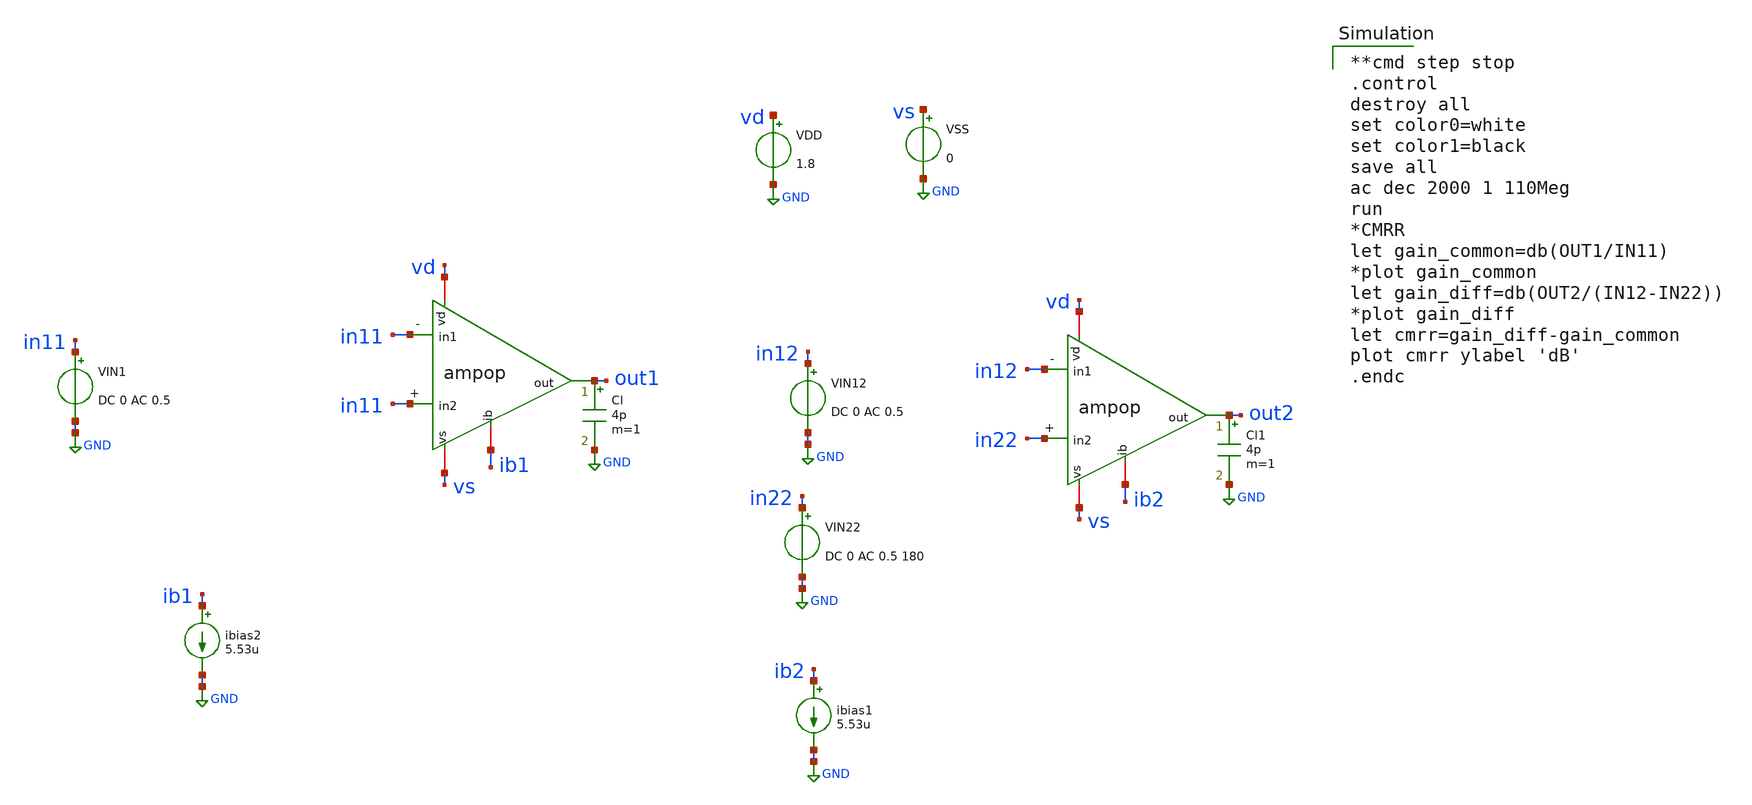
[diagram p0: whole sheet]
** sch_path: amp-op/xschem/ampop_tb-CMRR.sch
* Copyright 2020 Stefan Frederik Schippers
* Licensed under the Apache License, Version 2.0 (the "License");
* you may not use this file except in compliance with the License.
* You may obtain a copy of the License at
* https://www.apache.org/licenses/LICENSE-2.0
* Unless required by applicable law or agreed to in writing, software
* distributed under the License is distributed on an "AS IS" BASIS,
* WITHOUT WARRANTIES OR CONDITIONS OF ANY KIND, either express or implied.
* See the License for the specific language governing permissions and
* limitations under the License.
**.subckt ampop_tb-CMRR
ibias2 ib1 GND 5.53u
VDD vd GND 1.8
VSS vs GND 0
VIN12 in12 GND DC 0 AC 0.5
ibias1 ib2 GND 5.53u
VIN22 in22 GND DC 0 AC 0.5 180
Cl out1 GND 4p m=1
x1 vd in11 in11 out1 ib1 vs ampop
Cl1 out2 GND 4p m=1
x2 vd in12 in22 out2 ib2 vs ampop
VIN1 in11 GND DC 0 AC 0.5
**** begin user architecture code

**cmd step stop
.control
destroy all
set color0=white
set color1=black
save all
ac dec 2000 1 110Meg
run
*CMRR
let gain_common=db(OUT1/IN11)
*plot gain_common
let gain_diff=db(OUT2/(IN12-IN22))
*plot gain_diff
let cmrr=gain_diff-gain_common
plot cmrr ylabel 'dB'
.endc

 .lib $::SKYWATER_MODELS/sky130.lib.spice tt
.include $::SKYWATER_STDCELLS/sky130_fd_sc_hd.spice

**** end user architecture code
**.ends

* expanding   symbol:  /home/hugodg/projects-sky130/temp-sensor/amp-op/xschem/ampop.sym # of pins=6
** sym_path: amp-op/xschem/ampop.sym
** sch_path: amp-op/xschem/ampop.sch
.subckt ampop vd in1 in2 out ib vs
*.iopin vd
*.opin out
*.ipin in1
*.ipin in2
*.iopin vs
*.iopin ib
X1 vd net1 out ib vs buffer
X2 vd ib net1 in2 in1 vs ota
**** begin user architecture code


R0 in1 in1.t0 88.243
R1 in2 in2.t0 88.786
R2 vs.n0 vs.n4 362.164
R3 vs.n0 vs.n2 362.164
R4 vs.n30 vs.n25 181.834
R5 vs.n14 vs.n9 181.834
R6 vs.n18 vs.n17 108.422
R7 vs.n31 vs.n30 108.422
R8 vs.n0 vs.n6 108.422
R9 vs.n15 vs.n14 108.422
R10 vs.n34 vs.n5 5.045
R11 vs.n5 vs 0.812
R12 vs vs 0.431
R13 vs.n34 vs.n33 0.202
R14 vs vs.n34 0.182
R15 vs.n19 vs.n16 0.15
R16 vs.n32 vs.n23 0.062
R17 vs.n20 vs.n19 0.057
R18 vs.n16 vs.n7 0.055
R19 vs.n25 vs.n24 0.046
R20 vs.n9 vs.n8 0.046
R21 vs.n30 vs.n29 0.042
R22 vs.n14 vs.n13 0.042
R23 vs.n28 vs.n27 0.035
R24 vs.n12 vs.n11 0.035
R25 vs.n27 vs.n26 0.025
R26 vs.n11 vs.n10 0.025
R27 vs.n29 vs.n28 0.025
R28 vs.n13 vs.n12 0.025
R29 vs.n16 vs.n15 0.017
R30 vs.n19 vs.n18 0.017
R31 vs.n32 vs.n31 0.017
R32 vs.n4 vs.n3 0.013
R33 vs.n2 vs.n1 0.013
R34 vs.n7 vs.n0 0.007
R35 vs vs 0.005
R36 vs.n23 vs.n20 0.004
R37 vs.n33 vs.n32 0.003
R38 vs.n5 vs 0.002
R39 vs.n22 vs.n21 0.001
R40 vs.n23 vs.n22 0.001
R41 ib.n5 ib.t6 196.205
R42 ib.n6 ib.t5 196.185
R43 ib.n7 ib.t8 196.183
R44 ib.n8 ib.t7 196.181
R45 ib.n4 ib.t2 160.591
R46 ib.t2 ib.n3 160.08
R47 ib.n4 ib.t4 160.055
R48 ib.n0 ib.t9 24.837
R49 ib.n0 ib.t0 24.107
R50 ib.n1 ib.t1 17.747
R51 ib.n3 ib.t3 5.789
R52 ib.n2 ib.n1 4.041
R53 ib ib.n8 3.3
R54 ib.n5 ib.n4 1.125
R55 ib.n3 ib 0.407
R56 ib.n1 ib.n0 0.387
R57 ib.n6 ib.n5 0.175
R58 ib.n8 ib.n7 0.168
R59 ib.n7 ib.n6 0.162
R60 ib.n2 ib 0.113
R61 ib ib.n2 0.078
R62 vd.n74 vd.n73 5396.47
R63 vd.n63 vd.n62 3501.18
R64 vd.n84 vd.n83 3501.18
R65 vd.n62 vd.n59 909.81
R66 vd.n83 vd.n80 909.81
R67 vd.n65 vd.n64 722.167
R68 vd.n86 vd.n85 722.167
R69 vd.n71 vd.n70 575.623
R70 vd.n75 vd.n70 575.623
R71 vd.n74 vd.n69 569.784
R72 vd.n72 vd.n71 515.374
R73 vd.n53 vd.n52 379.482
R74 vd.n40 vd.n34 379.482
R75 vd.n61 vd.n60 373.458
R76 vd.n65 vd.n60 373.458
R77 vd.n82 vd.n81 373.458
R78 vd.n86 vd.n81 373.458
R79 vd.n69 vd.n68 326.776
R80 vd.n54 vd.n53 297.411
R81 vd.n41 vd.n40 297.411
R82 vd.n59 vd.n58 270.305
R83 vd.n80 vd.n79 270.305
R84 vd.n76 vd.n75 251.205
R85 vd.n71 vd.n68 248.846
R86 vd.n19 vd.n16 131.387
R87 vd.n4 vd.n1 131.387
R88 vd.n24 vd.n21 131.011
R89 vd.n9 vd.n6 131.011
R90 vd.n66 vd.n65 105.107
R91 vd.n87 vd.n86 105.107
R92 vd.n61 vd.n58 103.152
R93 vd.n82 vd.n79 103.152
R94 vd.n29 vd.n24 54.211
R95 vd.n14 vd.n9 54.211
R96 vd.n29 vd.n19 53.835
R97 vd.n14 vd.n4 53.835
R98 vd.n57 vd.n14 8.271
R99 vd.n57 vd.n29 7.938
R100 vd.n57 vd.n56 4.028
R101 vd.n91 vd.n90 1.897
R102 vd.n77 vd.n76 1.606
R103 vd.n67 vd.n66 1.199
R104 vd.n88 vd.n87 1.199
R105 vd.n91 vd.n57 1.058
R106 vd vd.n89 1.008
R107 vd.n78 vd.n77 0.975
R108 vd vd.n88 0.594
R109 vd.n77 vd.n68 0.389
R110 vd.n67 vd.n58 0.389
R111 vd.n88 vd.n79 0.334
R112 vd.n55 vd.n45 0.296
R113 vd.n89 vd.n78 0.273
R114 vd.n42 vd.n32 0.228
R115 vd.n56 vd.n55 0.18
R116 vd.n89 vd 0.173
R117 vd.n56 vd.n42 0.167
R118 vd.n19 vd.n18 0.161
R119 vd.n24 vd.n23 0.161
R120 vd.n4 vd.n3 0.161
R121 vd.n9 vd.n8 0.161
R122 vd.n23 vd.n22 0.139
R123 vd.n8 vd.n7 0.139
R124 vd.n18 vd.n17 0.139
R125 vd.n3 vd.n2 0.139
R126 vd.n90 vd 0.071
R127 vd.n78 vd.n67 0.054
R128 vd vd.n91 0.044
R129 vd.n90 vd 0.034
R130 vd.n42 vd.n41 0.017
R131 vd.n55 vd.n54 0.017
R132 vd.n62 vd.n61 0.015
R133 vd.n83 vd.n82 0.015
R134 vd.n16 vd.n15 0.015
R135 vd.n21 vd.n20 0.015
R136 vd.n1 vd.n0 0.015
R137 vd.n6 vd.n5 0.015
R138 vd.n52 vd.n51 0.013
R139 vd.n34 vd.n33 0.013
R140 vd.n26 vd.n25 0.013
R141 vd.n27 vd.n26 0.013
R142 vd.n11 vd.n10 0.013
R143 vd.n12 vd.n11 0.013
R144 vd.n75 vd.n74 0.004
R145 vd.n73 vd.n72 0.003
R146 vd.n63 vd.n60 0.003
R147 vd.n84 vd.n81 0.003
R148 vd.n53 vd.n50 0.003
R149 vd.n47 vd.n46 0.003
R150 vd.n36 vd.n35 0.003
R151 vd.n40 vd.n39 0.003
R152 vd.n64 vd.n63 0.003
R153 vd.n85 vd.n84 0.003
R154 vd.n50 vd.n49 0.003
R155 vd.n37 vd.n36 0.003
R156 vd.n48 vd.n47 0.003
R157 vd.n39 vd.n38 0.003
R158 vd.n73 vd.n70 0.003
R159 vd.n49 vd.n48 0.002
R160 vd.n38 vd.n37 0.002
R161 vd.n29 vd.n28 0.002
R162 vd.n28 vd.n27 0.002
R163 vd.n14 vd.n13 0.002
R164 vd.n13 vd.n12 0.002
R165 vd.n72 vd.n69 0.001
R166 vd.n64 vd.n59 0.001
R167 vd.n85 vd.n80 0.001
R168 vd.n32 vd.n31 0.001
R169 vd.n45 vd.n44 0.001
R170 vd.n44 vd.n43 0.001
R171 vd.n31 vd.n30 0.001
R172 vd.n76 vd.n69 0.001
R173 vd.n66 vd.n59 0.001
R174 vd.n87 vd.n80 0.001
R175 out.t0 out.n7 175.091
R176 out.n0 out.t2 175.044
R177 out.n2 out.n1 150.491
R178 out.n4 out.n3 150.491
R179 out.n6 out.n5 141.106
R180 out out.t0 28.743
R181 out.n5 out.t1 24.103
R182 out.n6 out.t7 24.103
R183 out.n4 out.t5 24.103
R184 out.n2 out.t3 24.102
R185 out.n0 out.t6 24.102
R186 out.n1 out.t9 24.102
R187 out.n3 out.t4 24.102
R188 out.n7 out.t8 24.102
R189 out.n7 out.n6 1.085
R190 out.n3 out.n2 0.988
R191 out.n5 out.n4 0.913
R192 out.n1 out.n0 0.863
R193 out out 0.023
R194 buffer_0/net1.n4 buffer_0/net1.t29 172.218
R195 buffer_0/net1.n5 buffer_0/net1.n4 149.523
R196 buffer_0/net1.n6 buffer_0/net1.n5 149.523
R197 buffer_0/net1.n7 buffer_0/net1.n6 149.523
R198 buffer_0/net1.n8 buffer_0/net1.n7 149.523
R199 buffer_0/net1.n9 buffer_0/net1.n8 149.523
R200 buffer_0/net1.n10 buffer_0/net1.n9 149.523
R201 buffer_0/net1.n11 buffer_0/net1.n10 149.523
R202 buffer_0/net1.n12 buffer_0/net1.n11 149.523
R203 buffer_0/net1.n13 buffer_0/net1.n12 149.523
R204 buffer_0/net1.n14 buffer_0/net1.n13 149.523
R205 buffer_0/net1.n15 buffer_0/net1.n14 149.523
R206 buffer_0/net1.n16 buffer_0/net1.n15 149.523
R207 buffer_0/net1.n17 buffer_0/net1.n16 149.523
R208 buffer_0/net1.n18 buffer_0/net1.n17 149.523
R209 buffer_0/net1.n19 buffer_0/net1.n18 149.523
R210 buffer_0/net1.n20 buffer_0/net1.n19 149.523
R211 buffer_0/net1.n21 buffer_0/net1.n20 149.523
R212 buffer_0/net1.n22 buffer_0/net1.n21 148.639
R213 buffer_0/net1.n22 buffer_0/net1.t16 24.284
R214 buffer_0/net1.n21 buffer_0/net1.t10 24.101
R215 buffer_0/net1.n20 buffer_0/net1.t27 24.101
R216 buffer_0/net1.n19 buffer_0/net1.t21 24.101
R217 buffer_0/net1.n18 buffer_0/net1.t4 24.101
R218 buffer_0/net1.n17 buffer_0/net1.t0 24.101
R219 buffer_0/net1.n16 buffer_0/net1.t22 24.101
R220 buffer_0/net1.n15 buffer_0/net1.t26 24.101
R221 buffer_0/net1.n14 buffer_0/net1.t18 24.101
R222 buffer_0/net1.n13 buffer_0/net1.t6 24.101
R223 buffer_0/net1.n12 buffer_0/net1.t23 24.101
R224 buffer_0/net1.n11 buffer_0/net1.t25 24.101
R225 buffer_0/net1.n10 buffer_0/net1.t8 24.101
R226 buffer_0/net1.n9 buffer_0/net1.t12 24.101
R227 buffer_0/net1.n8 buffer_0/net1.t28 24.101
R228 buffer_0/net1.n7 buffer_0/net1.t24 24.101
R229 buffer_0/net1.n6 buffer_0/net1.t14 24.101
R230 buffer_0/net1.n5 buffer_0/net1.t2 24.101
R231 buffer_0/net1.n4 buffer_0/net1.t20 24.101
R232 buffer_0/net1.n3 buffer_0/net1.t11 17.4
R233 buffer_0/net1.n3 buffer_0/net1.t17 17.4
R234 buffer_0/net1.n0 buffer_0/net1.t3 17.4
R235 buffer_0/net1.n0 buffer_0/net1.t15 17.4
R236 buffer_0/net1.n1 buffer_0/net1.t13 17.4
R237 buffer_0/net1.n1 buffer_0/net1.t9 17.4
R238 buffer_0/net1.n2 buffer_0/net1.t1 17.4
R239 buffer_0/net1.n2 buffer_0/net1.t5 17.4
R240 buffer_0/net1.n25 buffer_0/net1.t7 17.4
R241 buffer_0/net1.n25 buffer_0/net1.t19 17.4
R242 buffer_0/net1.n24 buffer_0/net1.n23 3.481
R243 buffer_0/net1 buffer_0/net1.n0 3.306
R244 buffer_0/net1.n27 buffer_0/net1.n26 3.218
R245 buffer_0/net1.n26 buffer_0/net1.n24 3.218
R246 buffer_0/net1.n23 buffer_0/net1.n22 1.24
R247 buffer_0/net1.n27 buffer_0/net1.n1 0.931
R248 buffer_0/net1.n24 buffer_0/net1.n2 0.931
R249 buffer_0/net1.n26 buffer_0/net1.n25 0.931
R250 buffer_0/net1 buffer_0/net1.n27 0.843
R251 buffer_0/net1.n23 buffer_0/net1.n3 0.389
C0 ota_0/m1_1300_5200# ota_0/out -0.03fF
C1 buffer_0/net2 vd 0.01fF
C2 ota_0/out vd 0.05fF
C3 buffer_0/net1.t3 vs 0.02fF
C4 buffer_0/net1.t15 vs 0.02fF
C5 buffer_0/net1.n0 vs 0.31fF $ **FLOATING
C6 buffer_0/net1.t13 vs 0.02fF
C7 buffer_0/net1.t9 vs 0.02fF
C8 buffer_0/net1.n1 vs 0.19fF $ **FLOATING
C9 buffer_0/net1.t1 vs 0.02fF
C10 buffer_0/net1.t5 vs 0.02fF
C11 buffer_0/net1.n2 vs 0.19fF $ **FLOATING
C12 buffer_0/net1.t11 vs 0.02fF
C13 buffer_0/net1.t17 vs 0.02fF
C14 buffer_0/net1.n3 vs 0.15fF $ **FLOATING
C15 buffer_0/net1.t10 vs 0.47fF
C16 buffer_0/net1.t27 vs 0.47fF
C17 buffer_0/net1.t21 vs 0.47fF
C18 buffer_0/net1.t4 vs 0.47fF
C19 buffer_0/net1.t0 vs 0.47fF
C20 buffer_0/net1.t22 vs 0.47fF
C21 buffer_0/net1.t26 vs 0.47fF
C22 buffer_0/net1.t18 vs 0.47fF
C23 buffer_0/net1.t6 vs 0.47fF
C24 buffer_0/net1.t23 vs 0.47fF
C25 buffer_0/net1.t25 vs 0.47fF
C26 buffer_0/net1.t8 vs 0.47fF
C27 buffer_0/net1.t12 vs 0.47fF
C28 buffer_0/net1.t28 vs 0.47fF
C29 buffer_0/net1.t24 vs 0.47fF
C30 buffer_0/net1.t14 vs 0.47fF
C31 buffer_0/net1.t2 vs 0.47fF
C32 buffer_0/net1.t20 vs 0.47fF
C33 buffer_0/net1.t29 vs 0.75fF
C34 buffer_0/net1.n4 vs 0.39fF $ **FLOATING
C35 buffer_0/net1.n5 vs 0.34fF $ **FLOATING
C36 buffer_0/net1.n6 vs 0.34fF $ **FLOATING
C37 buffer_0/net1.n7 vs 0.34fF $ **FLOATING
C38 buffer_0/net1.n8 vs 0.34fF $ **FLOATING
C39 buffer_0/net1.n9 vs 0.34fF $ **FLOATING
C40 buffer_0/net1.n10 vs 0.34fF $ **FLOATING
C41 buffer_0/net1.n11 vs 0.34fF $ **FLOATING
C42 buffer_0/net1.n12 vs 0.34fF $ **FLOATING
C43 buffer_0/net1.n13 vs 0.34fF $ **FLOATING
C44 buffer_0/net1.n14 vs 0.34fF $ **FLOATING
C45 buffer_0/net1.n15 vs 0.34fF $ **FLOATING
C46 buffer_0/net1.n16 vs 0.34fF $ **FLOATING
C47 buffer_0/net1.n17 vs 0.34fF $ **FLOATING
C48 buffer_0/net1.n18 vs 0.34fF $ **FLOATING
C49 buffer_0/net1.n19 vs 0.34fF $ **FLOATING
C50 buffer_0/net1.n20 vs 0.34fF $ **FLOATING
C51 buffer_0/net1.n21 vs 0.34fF $ **FLOATING
C52 buffer_0/net1.t16 vs 0.47fF
C53 buffer_0/net1.n22 vs 0.21fF $ **FLOATING
C54 buffer_0/net1.n23 vs 1.22fF $ **FLOATING
C55 buffer_0/net1.n24 vs 4.35fF $ **FLOATING
C56 buffer_0/net1.t7 vs 0.02fF
C57 buffer_0/net1.t19 vs 0.02fF
C58 buffer_0/net1.n25 vs 0.19fF $ **FLOATING
C59 buffer_0/net1.n26 vs 0.36fF $ **FLOATING
C60 buffer_0/net1.n27 vs 0.25fF $ **FLOATING
C61 out.t8 vs 0.59fF
C62 out.t1 vs 0.59fF
C63 out.t4 vs 0.59fF
C64 out.t9 vs 0.59fF
C65 out.t2 vs 0.94fF
C66 out.t6 vs 0.59fF
C67 out.n0 vs 2.69fF $ **FLOATING
C68 out.n1 vs 2.83fF $ **FLOATING
C69 out.t3 vs 0.59fF
C70 out.n2 vs 0.86fF $ **FLOATING
C71 out.n3 vs 0.86fF $ **FLOATING
C72 out.t5 vs 0.59fF
C73 out.n4 vs 0.91fF $ **FLOATING
C74 out.n5 vs 0.92fF $ **FLOATING
C75 out.t7 vs 0.59fF
C76 out.n6 vs 0.84fF $ **FLOATING
C77 out.n7 vs 0.91fF $ **FLOATING
C78 out.t0 vs 0.89fF
C79 vd.n0 vs 0.34fF $ **FLOATING
C80 vd.n1 vs 0.06fF $ **FLOATING
C81 vd.n2 vs 0.33fF $ **FLOATING
C82 vd.n3 vs 0.04fF $ **FLOATING
C83 vd.n4 vs 0.04fF $ **FLOATING
C84 vd.n5 vs 0.34fF $ **FLOATING
C85 vd.n6 vs 0.06fF $ **FLOATING
C86 vd.n7 vs 0.33fF $ **FLOATING
C87 vd.n8 vs 0.04fF $ **FLOATING
C88 vd.n9 vs 0.04fF $ **FLOATING
C89 vd.n10 vs 0.07fF $ **FLOATING
C90 vd.n11 vs 0.07fF $ **FLOATING
C91 vd.n12 vs 0.35fF $ **FLOATING
C92 vd.n13 vs 0.02fF $ **FLOATING
C93 vd.n14 vs 0.49fF $ **FLOATING
C94 vd.n15 vs 0.34fF $ **FLOATING
C95 vd.n16 vs 0.06fF $ **FLOATING
C96 vd.n17 vs 0.33fF $ **FLOATING
C97 vd.n18 vs 0.04fF $ **FLOATING
C98 vd.n19 vs 0.04fF $ **FLOATING
C99 vd.n20 vs 0.34fF $ **FLOATING
C100 vd.n21 vs 0.06fF $ **FLOATING
C101 vd.n22 vs 0.33fF $ **FLOATING
C102 vd.n23 vs 0.04fF $ **FLOATING
C103 vd.n24 vs 0.04fF $ **FLOATING
C104 vd.n25 vs 0.07fF $ **FLOATING
C105 vd.n26 vs 0.07fF $ **FLOATING
C106 vd.n27 vs 0.35fF $ **FLOATING
C107 vd.n28 vs 0.02fF $ **FLOATING
C108 vd.n29 vs 0.51fF $ **FLOATING
C109 vd.n30 vs 1.30fF $ **FLOATING
C110 vd.n31 vs 0.03fF $ **FLOATING
C111 vd.n32 vs 0.64fF $ **FLOATING
C112 vd.n33 vs 1.30fF $ **FLOATING
C113 vd.n34 vs 0.15fF $ **FLOATING
C114 vd.n35 vs 0.13fF $ **FLOATING
C115 vd.n36 vs 0.14fF $ **FLOATING
C116 vd.n37 vs 1.01fF $ **FLOATING
C117 vd.n38 vs 1.01fF $ **FLOATING
C118 vd.n39 vs 0.14fF $ **FLOATING
C119 vd.n40 vs 0.13fF $ **FLOATING
C120 vd.n41 vs 0.07fF $ **FLOATING
C121 vd.n42 vs 0.10fF $ **FLOATING
C122 vd.n43 vs 1.30fF $ **FLOATING
C123 vd.n44 vs 0.03fF $ **FLOATING
C124 vd.n45 vs 0.34fF $ **FLOATING
C125 vd.n46 vs 0.13fF $ **FLOATING
C126 vd.n47 vs 0.14fF $ **FLOATING
C127 vd.n48 vs 1.01fF $ **FLOATING
C128 vd.n49 vs 1.01fF $ **FLOATING
C129 vd.n50 vs 0.14fF $ **FLOATING
C130 vd.n51 vs 1.30fF $ **FLOATING
C131 vd.n52 vs 0.15fF $ **FLOATING
C132 vd.n53 vs 0.13fF $ **FLOATING
C133 vd.n54 vs 0.07fF $ **FLOATING
C134 vd.n55 vs 0.35fF $ **FLOATING
C135 vd.n56 vs 1.41fF $ **FLOATING
C136 vd.n57 vs 13.41fF $ **FLOATING
C137 vd.n58 vs 0.09fF $ **FLOATING
C138 vd.n59 vs 2.13fF $ **FLOATING
C139 vd.n60 vs 0.14fF $ **FLOATING
C140 vd.n61 vs 0.09fF $ **FLOATING
C141 vd.n62 vs 1.22fF $ **FLOATING
C142 vd.n63 vs 0.14fF $ **FLOATING
C143 vd.n65 vs 1.31fF $ **FLOATING
C144 vd.n66 vs 0.26fF $ **FLOATING
C145 vd.n67 vs 0.81fF $ **FLOATING
C146 vd.n68 vs 0.13fF $ **FLOATING
C147 vd.n69 vs 5.56fF $ **FLOATING
C148 vd.n70 vs 0.22fF $ **FLOATING
C149 vd.n71 vs 3.29fF $ **FLOATING
C150 vd.n73 vs 0.22fF $ **FLOATING
C151 vd.n74 vs 3.13fF $ **FLOATING
C152 vd.n75 vs 0.16fF $ **FLOATING
C153 vd.n76 vs 0.34fF $ **FLOATING
C154 vd.n77 vs 3.07fF $ **FLOATING
C155 vd.n78 vs 0.50fF $ **FLOATING
C156 vd.n79 vs 0.09fF $ **FLOATING
C157 vd.n80 vs 2.13fF $ **FLOATING
C158 vd.n81 vs 0.14fF $ **FLOATING
C159 vd.n82 vs 0.09fF $ **FLOATING
C160 vd.n83 vs 1.22fF $ **FLOATING
C161 vd.n84 vs 0.14fF $ **FLOATING
C162 vd.n86 vs 1.31fF $ **FLOATING
C163 vd.n87 vs 0.26fF $ **FLOATING
C164 vd.n88 vs 1.13fF $ **FLOATING
C165 vd.n89 vs 1.25fF $ **FLOATING
C166 vd.n90 vs 1.36fF $ **FLOATING
C167 vd.n91 vs 1.49fF $ **FLOATING
C168 ib.t1 vs 0.01fF
C169 ib.t9 vs 0.19fF
C170 ib.t0 vs 0.19fF
C171 ib.n0 vs 0.26fF $ **FLOATING
C172 ib.n1 vs 0.16fF $ **FLOATING
C173 ib.n2 vs 0.12fF $ **FLOATING
C174 ib.t8 vs 0.81fF
C175 ib.t5 vs 0.81fF
C176 ib.t6 vs 0.81fF
C177 ib.t4 vs 0.68fF
C178 ib.t3 vs 0.12fF
C179 ib.n3 vs 1.03fF $ **FLOATING
C180 ib.t2 vs 0.41fF
C181 ib.n4 vs 1.75fF $ **FLOATING
C182 ib.n5 vs 0.99fF $ **FLOATING
C183 ib.n6 vs 0.51fF $ **FLOATING
C184 ib.n7 vs 0.52fF $ **FLOATING
C185 ib.t7 vs 0.81fF
C186 ib.n8 vs 1.32fF $ **FLOATING
C187 buffer_0/net4 vs 1.11fF
C188 out vs 13.18fF
C189 buffer_0/net3 vs 2.90fF
C190 vd vs 38.03fF
C191 buffer_0/net1 vs 14.70fF
C192 buffer_0/net2 vs 3.06fF
C193 ota_0/out vs 11.16fF
C194 ota_0/m1_n20_5200# vs 2.40fF
C195 ota_0/m1_420_6300# vs 4.72fF
C196 ota_0/m1_1300_5200# vs 14.02fF


**** end user architecture code
.ends


* expanding   symbol:  /home/hugodg/projects-sky130/temp-sensor/amp-op/xschem/buffer.sym # of pins=5
** sym_path: buffer/xschem/buffer.sym
** sch_path: buffer/xschem/buffer.sch
.subckt buffer vd in out ib gnd
*.iopin vd
*.iopin ib
*.iopin out
*.iopin in
*.iopin gnd
XM3 net2 net2 vd vd sky130_fd_pr__pfet_01v8 L=1 W=1 nf=1 ad='int((nf+1)/2) * W/nf * 0.29' as='int((nf+2)/2) * W/nf * 0.29'
+ pd='2*int((nf+1)/2) * (W/nf + 0.29)' ps='2*int((nf+2)/2) * (W/nf + 0.29)' nrd='0.29 / W' nrs='0.29 / W'
+ sa=0 sb=0 sd=0 mult=1 m=1
XM1 net2 out net4 gnd sky130_fd_pr__nfet_01v8 L=1 W=10 nf=10 ad='int((nf+1)/2) * W/nf * 0.29' as='int((nf+2)/2) * W/nf * 0.29'
+ pd='2*int((nf+1)/2) * (W/nf + 0.29)' ps='2*int((nf+2)/2) * (W/nf + 0.29)' nrd='0.29 / W' nrs='0.29 / W'
+ sa=0 sb=0 sd=0 mult=1 m=1
XM2 net3 in net4 gnd sky130_fd_pr__nfet_01v8 L=1 W=10 nf=10 ad='int((nf+1)/2) * W/nf * 0.29' as='int((nf+2)/2) * W/nf * 0.29'
+ pd='2*int((nf+1)/2) * (W/nf + 0.29)' ps='2*int((nf+2)/2) * (W/nf + 0.29)' nrd='0.29 / W' nrs='0.29 / W'
+ sa=0 sb=0 sd=0 mult=1 m=1
XM4 net3 net3 vd vd sky130_fd_pr__pfet_01v8 L=1 W=1 nf=1 ad='int((nf+1)/2) * W/nf * 0.29' as='int((nf+2)/2) * W/nf * 0.29'
+ pd='2*int((nf+1)/2) * (W/nf + 0.29)' ps='2*int((nf+2)/2) * (W/nf + 0.29)' nrd='0.29 / W' nrs='0.29 / W'
+ sa=0 sb=0 sd=0 mult=1 m=1
XM5 net4 ib gnd gnd sky130_fd_pr__nfet_01v8 L=1 W=1 nf=1 ad='int((nf+1)/2) * W/nf * 0.29' as='int((nf+2)/2) * W/nf * 0.29'
+ pd='2*int((nf+1)/2) * (W/nf + 0.29)' ps='2*int((nf+2)/2) * (W/nf + 0.29)' nrd='0.29 / W' nrs='0.29 / W'
+ sa=0 sb=0 sd=0 mult=1 m=1
XM6 out net3 vd vd sky130_fd_pr__pfet_01v8 L=1 W=10 nf=10 ad='int((nf+1)/2) * W/nf * 0.29' as='int((nf+2)/2) * W/nf * 0.29'
+ pd='2*int((nf+1)/2) * (W/nf + 0.29)' ps='2*int((nf+2)/2) * (W/nf + 0.29)' nrd='0.29 / W' nrs='0.29 / W'
+ sa=0 sb=0 sd=0 mult=1 m=1
XM7 out net1 gnd gnd sky130_fd_pr__nfet_01v8 L=1 W=10 nf=10 ad='int((nf+1)/2) * W/nf * 0.29' as='int((nf+2)/2) * W/nf * 0.29'
+ pd='2*int((nf+1)/2) * (W/nf + 0.29)' ps='2*int((nf+2)/2) * (W/nf + 0.29)' nrd='0.29 / W' nrs='0.29 / W'
+ sa=0 sb=0 sd=0 mult=1 m=1
XM8 net1 net2 vd vd sky130_fd_pr__pfet_01v8 L=1 W=10 nf=10 ad='int((nf+1)/2) * W/nf * 0.29' as='int((nf+2)/2) * W/nf * 0.29'
+ pd='2*int((nf+1)/2) * (W/nf + 0.29)' ps='2*int((nf+2)/2) * (W/nf + 0.29)' nrd='0.29 / W' nrs='0.29 / W'
+ sa=0 sb=0 sd=0 mult=1 m=1
XM9 net1 net1 gnd gnd sky130_fd_pr__nfet_01v8 L=1 W=10 nf=10 ad='int((nf+1)/2) * W/nf * 0.29' as='int((nf+2)/2) * W/nf * 0.29'
+ pd='2*int((nf+1)/2) * (W/nf + 0.29)' ps='2*int((nf+2)/2) * (W/nf + 0.29)' nrd='0.29 / W' nrs='0.29 / W'
+ sa=0 sb=0 sd=0 mult=1 m=1
XM10 ib ib gnd gnd sky130_fd_pr__nfet_01v8 L=1 W=1 nf=1 ad='int((nf+1)/2) * W/nf * 0.29' as='int((nf+2)/2) * W/nf * 0.29'
+ pd='2*int((nf+1)/2) * (W/nf + 0.29)' ps='2*int((nf+2)/2) * (W/nf + 0.29)' nrd='0.29 / W' nrs='0.29 / W'
+ sa=0 sb=0 sd=0 mult=1 m=1
XPD1 net8 net7 net6 net5 sky130_fd_pr__pfet_01v8 L=1 W=1 nf=1 ad='int((nf+1)/2) * W/nf * 0.29' as='int((nf+2)/2) * W/nf * 0.29'
+ pd='2*int((nf+1)/2) * (W/nf + 0.29)' ps='2*int((nf+2)/2) * (W/nf + 0.29)' nrd='0.29 / W' nrs='0.29 / W'
+ sa=0 sb=0 sd=0 mult=1 m=1
XPD2 net12 net11 net10 net9 sky130_fd_pr__pfet_01v8 L=1 W=1 nf=1 ad='int((nf+1)/2) * W/nf * 0.29' as='int((nf+2)/2) * W/nf * 0.29'
+ pd='2*int((nf+1)/2) * (W/nf + 0.29)' ps='2*int((nf+2)/2) * (W/nf + 0.29)' nrd='0.29 / W' nrs='0.29 / W'
+ sa=0 sb=0 sd=0 mult=1 m=1
XPD3 net16 net15 net14 net13 sky130_fd_pr__pfet_01v8 L=1 W=1 nf=1 ad='int((nf+1)/2) * W/nf * 0.29' as='int((nf+2)/2) * W/nf * 0.29'
+ pd='2*int((nf+1)/2) * (W/nf + 0.29)' ps='2*int((nf+2)/2) * (W/nf + 0.29)' nrd='0.29 / W' nrs='0.29 / W'
+ sa=0 sb=0 sd=0 mult=1 m=1
XPD4 net20 net19 net18 net17 sky130_fd_pr__pfet_01v8 L=1 W=1 nf=1 ad='int((nf+1)/2) * W/nf * 0.29' as='int((nf+2)/2) * W/nf * 0.29'
+ pd='2*int((nf+1)/2) * (W/nf + 0.29)' ps='2*int((nf+2)/2) * (W/nf + 0.29)' nrd='0.29 / W' nrs='0.29 / W'
+ sa=0 sb=0 sd=0 mult=1 m=1
XND1 net25 net21 net26 gnd sky130_fd_pr__nfet_01v8 L=1 W=1 nf=1 ad='int((nf+1)/2) * W/nf * 0.29' as='int((nf+2)/2) * W/nf * 0.29'
+ pd='2*int((nf+1)/2) * (W/nf + 0.29)' ps='2*int((nf+2)/2) * (W/nf + 0.29)' nrd='0.29 / W' nrs='0.29 / W'
+ sa=0 sb=0 sd=0 mult=1 m=1
XND2 net27 net22 net28 gnd sky130_fd_pr__nfet_01v8 L=1 W=1 nf=1 ad='int((nf+1)/2) * W/nf * 0.29' as='int((nf+2)/2) * W/nf * 0.29'
+ pd='2*int((nf+1)/2) * (W/nf + 0.29)' ps='2*int((nf+2)/2) * (W/nf + 0.29)' nrd='0.29 / W' nrs='0.29 / W'
+ sa=0 sb=0 sd=0 mult=1 m=1
XND3 net29 net23 net30 gnd sky130_fd_pr__nfet_01v8 L=1 W=1 nf=1 ad='int((nf+1)/2) * W/nf * 0.29' as='int((nf+2)/2) * W/nf * 0.29'
+ pd='2*int((nf+1)/2) * (W/nf + 0.29)' ps='2*int((nf+2)/2) * (W/nf + 0.29)' nrd='0.29 / W' nrs='0.29 / W'
+ sa=0 sb=0 sd=0 mult=1 m=1
XND4 net32 net24 net31 gnd sky130_fd_pr__nfet_01v8 L=1 W=1 nf=1 ad='int((nf+1)/2) * W/nf * 0.29' as='int((nf+2)/2) * W/nf * 0.29'
+ pd='2*int((nf+1)/2) * (W/nf + 0.29)' ps='2*int((nf+2)/2) * (W/nf + 0.29)' nrd='0.29 / W' nrs='0.29 / W'
+ sa=0 sb=0 sd=0 mult=1 m=1
.ends


* expanding   symbol:  /home/hugodg/projects-sky130/temp-sensor/amp-op/xschem/ota.sym # of pins=6
** sym_path: amp-op/xschem/ota.sym
** sch_path: amp-op/xschem/ota.sch
.subckt ota vd ib out in2 in1 vs
*.iopin vd
*.iopin vs
*.iopin ib
*.ipin in1
*.ipin in2
*.opin out
XCC out d sky130_fd_pr__cap_mim_m3_1 W=21 L=21 MF=1 m=1
XM5 ib ib vd vd sky130_fd_pr__pfet_01v8 L=1 W=6 nf=1 ad='int((nf+1)/2) * W/nf * 0.29' as='int((nf+2)/2) * W/nf * 0.29'
+ pd='2*int((nf+1)/2) * (W/nf + 0.29)' ps='2*int((nf+2)/2) * (W/nf + 0.29)' nrd='0.29 / W' nrs='0.29 / W'
+ sa=0 sb=0 sd=0 mult=1 m=1
XM6 b ib vd vd sky130_fd_pr__pfet_01v8 L=1 W=6 nf=1 ad='int((nf+1)/2) * W/nf * 0.29' as='int((nf+2)/2) * W/nf * 0.29'
+ pd='2*int((nf+1)/2) * (W/nf + 0.29)' ps='2*int((nf+2)/2) * (W/nf + 0.29)' nrd='0.29 / W' nrs='0.29 / W'
+ sa=0 sb=0 sd=0 mult=1 m=1
XM8 out ib vd vd sky130_fd_pr__pfet_01v8 L=1 W=30 nf=4 ad='int((nf+1)/2) * W/nf * 0.29' as='int((nf+2)/2) * W/nf * 0.29'
+ pd='2*int((nf+1)/2) * (W/nf + 0.29)' ps='2*int((nf+2)/2) * (W/nf + 0.29)' nrd='0.29 / W' nrs='0.29 / W'
+ sa=0 sb=0 sd=0 mult=1 m=1
XM1 c in1 b b sky130_fd_pr__pfet_01v8 L=1 W=3 nf=1 ad='int((nf+1)/2) * W/nf * 0.29' as='int((nf+2)/2) * W/nf * 0.29'
+ pd='2*int((nf+1)/2) * (W/nf + 0.29)' ps='2*int((nf+2)/2) * (W/nf + 0.29)' nrd='0.29 / W' nrs='0.29 / W'
+ sa=0 sb=0 sd=0 mult=1 m=1
XM2 d in2 b b sky130_fd_pr__pfet_01v8 L=1 W=3 nf=1 ad='int((nf+1)/2) * W/nf * 0.29' as='int((nf+2)/2) * W/nf * 0.29'
+ pd='2*int((nf+1)/2) * (W/nf + 0.29)' ps='2*int((nf+2)/2) * (W/nf + 0.29)' nrd='0.29 / W' nrs='0.29 / W'
+ sa=0 sb=0 sd=0 mult=1 m=1
XM3 c c vs vs sky130_fd_pr__nfet_01v8 L=1 W=1 nf=1 ad='int((nf+1)/2) * W/nf * 0.29' as='int((nf+2)/2) * W/nf * 0.29'
+ pd='2*int((nf+1)/2) * (W/nf + 0.29)' ps='2*int((nf+2)/2) * (W/nf + 0.29)' nrd='0.29 / W' nrs='0.29 / W'
+ sa=0 sb=0 sd=0 mult=1 m=1
XM4 d c vs vs sky130_fd_pr__nfet_01v8 L=1 W=1 nf=1 ad='int((nf+1)/2) * W/nf * 0.29' as='int((nf+2)/2) * W/nf * 0.29'
+ pd='2*int((nf+1)/2) * (W/nf + 0.29)' ps='2*int((nf+2)/2) * (W/nf + 0.29)' nrd='0.29 / W' nrs='0.29 / W'
+ sa=0 sb=0 sd=0 mult=1 m=1
XM7 out d vs vs sky130_fd_pr__nfet_01v8 L=1 W=9 nf=2 ad='int((nf+1)/2) * W/nf * 0.29' as='int((nf+2)/2) * W/nf * 0.29'
+ pd='2*int((nf+1)/2) * (W/nf + 0.29)' ps='2*int((nf+2)/2) * (W/nf + 0.29)' nrd='0.29 / W' nrs='0.29 / W'
+ sa=0 sb=0 sd=0 mult=1 m=1
.ends

.GLOBAL GND
.end
